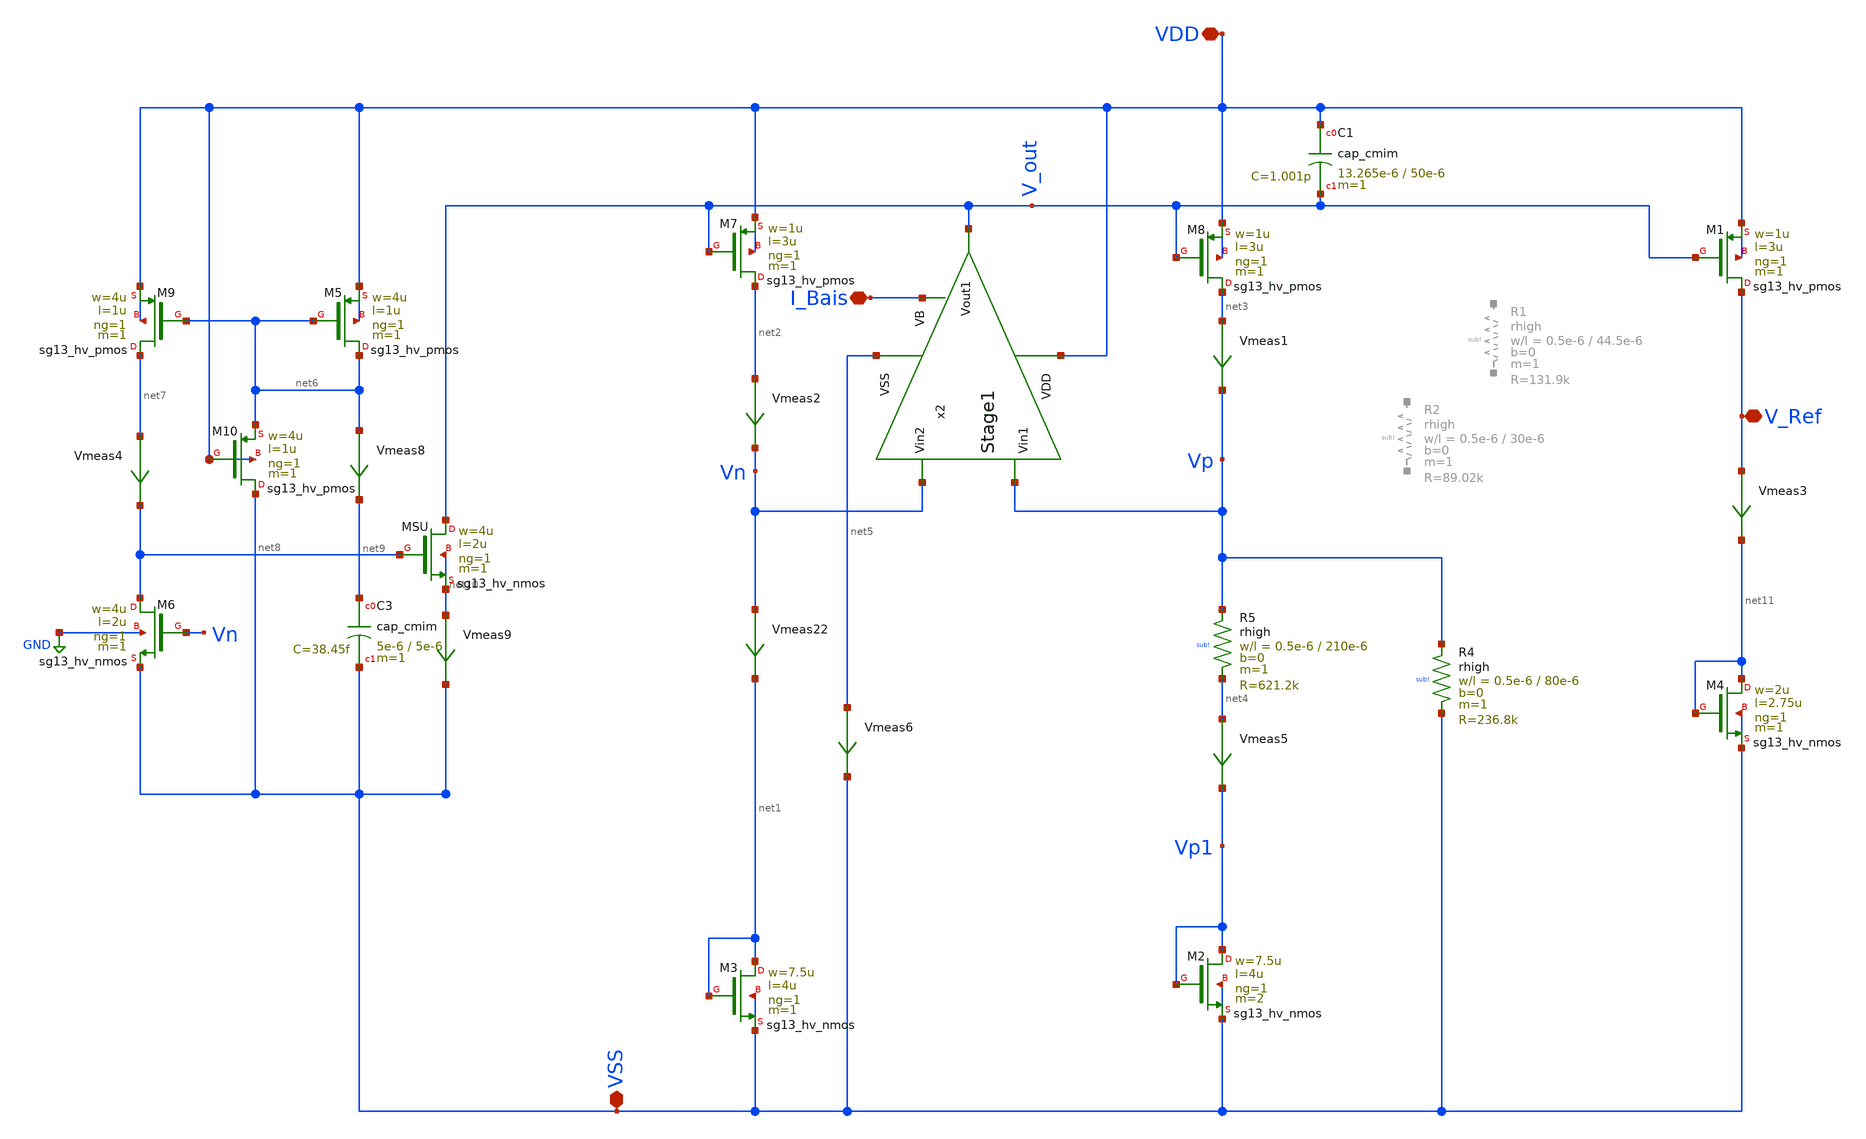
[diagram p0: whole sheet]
** sch_path: dependencies/PMU/PMU-main/schematic/xschem/BGR_I_ZTAT.sch
**.subckt BGR_I_ZTAT VDD I_Bais V_Ref VSS
*.iopin VDD
*.iopin I_Bais
*.iopin V_Ref
*.iopin VSS
XM7 net2 V_out VDD VDD sg13_hv_pmos w=1u l=3u ng=1 m=1 mm_ok=1
XM8 net3 V_out VDD VDD sg13_hv_pmos w=1u l=3u ng=1 m=1 mm_ok=1
XC1 VDD V_out cap_cmim w=13.265e-6 l=50e-6 m=1 mm_ok=1
Vmeas1 net3 Vp 0
.save i(vmeas1)
Vmeas22 Vn net1 0
.save i(vmeas22)
x2 VDD I_Bais Vp Vn V_out net5 Stage1
XM2 Vp1 Vp1 VSS VSS sg13_hv_nmos w=7.5u l=4u ng=1 m=2 mm_ok=1
XM3 net1 net1 VSS VSS sg13_hv_nmos w=7.5u l=4u ng=1 m=1 mm_ok=1
Vmeas2 net2 Vn 0
.save i(vmeas2)
Vmeas5 net4 Vp1 0
.save i(vmeas5)
Vmeas6 net5 VSS 0
.save i(vmeas6)
XM1 V_Ref V_out VDD VDD sg13_hv_pmos w=1u l=3u ng=1 m=1 mm_ok=1
Vmeas3 V_Ref net11 0
.save i(vmeas3)
XM4 net11 net11 VSS VSS sg13_hv_nmos w=2u l=2.75u ng=1 m=1 mm_ok=1
XM6 net8 Vn VSS GND sg13_hv_nmos w=4u l=2u ng=1 m=1 mm_ok=1
XM5 net6 net6 VDD VDD sg13_hv_pmos w=4u l=1u ng=1 m=1 mm_ok=1
XM9 net7 net6 VDD VDD sg13_hv_pmos w=4u l=1u ng=1 m=1 mm_ok=1
Vmeas4 net7 net8 0
.save i(vmeas4)
XC3 net9 VSS cap_cmim w=5e-6 l=5e-6 m=1 mm_ok=1
XM10 VSS VDD net6 VDD sg13_hv_pmos w=4u l=1u ng=1 m=1 mm_ok=1
XMSU V_out net8 net10 net10 sg13_hv_nmos w=4u l=2u ng=1 m=1 mm_ok=1
Vmeas8 net6 net9 0
.save i(vmeas8)
Vmeas9 net10 VSS 0
.save i(vmeas9)
XR4 Vp VSS sub! rhigh w=0.5e-6 l=80e-6 m=1 b=0 mm_ok=1
XR5 Vp net4 sub! rhigh w=0.5e-6 l=210e-6 m=1 b=0 mm_ok=1
**.ends

* expanding   symbol:  Stage1.sym # of pins=6
** sym_path: dependencies/PMU/PMU-main/schematic/xschem/Stage1.sym
** sch_path: dependencies/PMU/PMU-main/schematic/xschem/Stage1.sch
.subckt Stage1 VDD VB Vin1 Vin2 Vout1 VSS
*.iopin VDD
*.ipin VB
*.ipin Vin1
*.ipin Vin2
*.iopin VSS
*.opin Vout1
XM1 net1 Vin1 VX VDD sg13_hv_pmos w=10u l=5u ng=2 m=2 mm_ok=1
XM2 net1 net1 VSS VSS sg13_hv_nmos w=1u l=10u ng=2 m=2 mm_ok=1
XM3 Vout1 net1 VSS VSS sg13_hv_nmos w=1u l=10u ng=2 m=2 mm_ok=1
XM4 Vout1 Vin2 VX VDD sg13_hv_pmos w=10u l=5u ng=2 m=2 mm_ok=1
XM5 VX VB VDD VDD sg13_hv_pmos w=10u l=2u ng=1 m=5 mm_ok=1
.ends

.GLOBAL GND
.end
